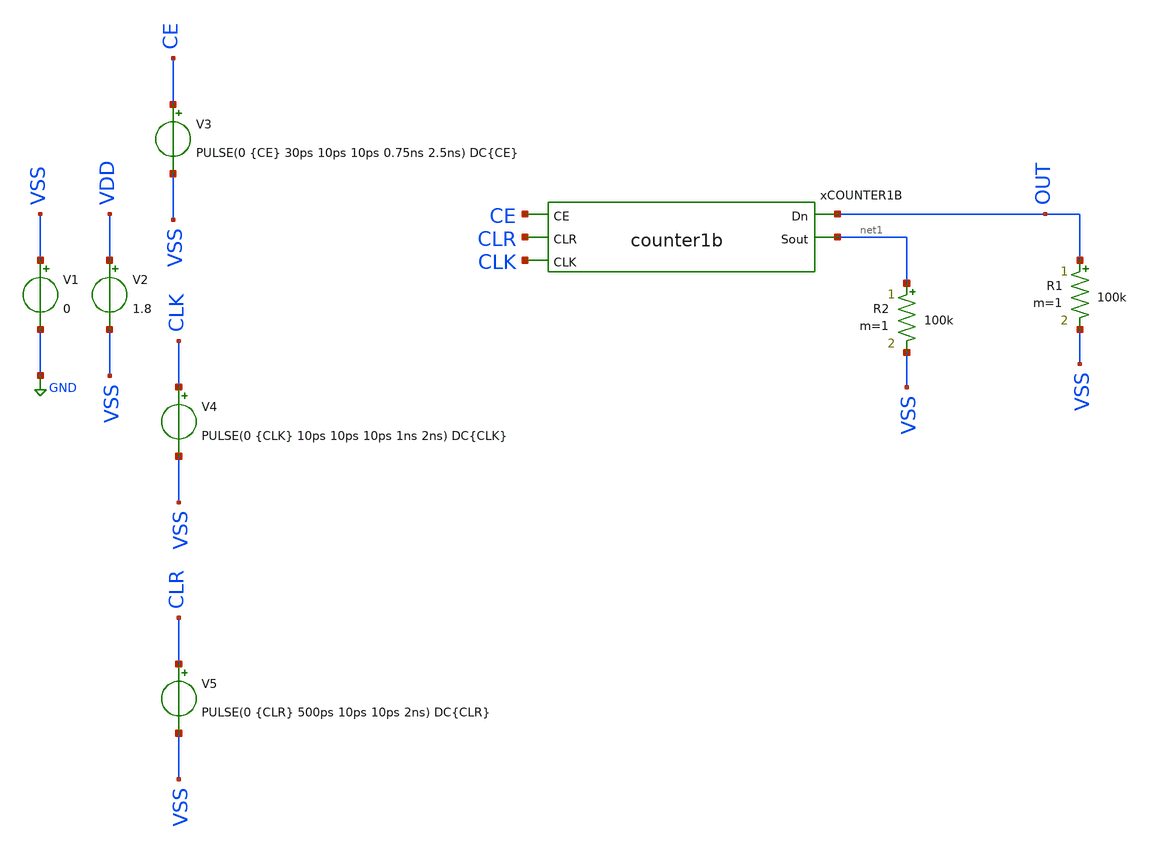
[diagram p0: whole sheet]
** sch_path: track_vlsi/scandaliaris/sch/tb_counter1b.sch
**.subckt tb_counter1b
V1 VSS GND 0
V2 VDD VSS 1.8
V3 CE VSS PULSE(0 {CE} 30ps 10ps 10ps 0.75ns 2.5ns) DC{CE}

V4 CLK VSS PULSE(0 {CLK} 10ps 10ps 10ps 1ns 2ns) DC{CLK}

R1 OUT VSS 100k m=1
V5 CLR VSS PULSE(0 {CLR} 500ps 10ps 10ps 2ns) DC{CLR}
xCOUNTER1B OUT CE CLR CLK net1 VSS VDD counter1b
R2 net1 VSS 100k m=1
**** begin user architecture code


* Parametros del circuito
.param CE = 1.8
.param CLK = 1.8
.param CLR = 1.8
.options TEMP = 27.0

* Include
.lib /home/eamta/skywater/skywater-pdk/libraries/sky130_fd_pr_ngspice/latest/models/corners/sky130.lib TT

* Signals to SAVE
.save all
 + @M.X1.XM1.msky130_fd_pr__nfet_01v8[id]
 + @M.X1.XM1.msky130_fd_pr__nfet_01v8[gm]
 + @M.X1.XM2.msky130_fd_pr__pfet_01v8[id]
 + @M.X1.XM2.msky130_fd_pr__pfet_01v8[gm]

* Simulation
.control
  tran .05n 20ns
  setplot tran1
  plot v(OUT) v(CE) v(CLK) v(CLR)
  *set plot tran2
  *plot @M.X1.XM1.msky130_fd_pr__nfet_01v8[id] @M.X1.XM2.msky130_fd_pr__pfet_01v8[id]
  *set plot tran3
  *plot @M.X1.XM1.msky130_fd_pr__nfet_01v8[gm] @M.X1.XM2.msky130_fd_pr__pfet_01v8[gm]
  *set filetype=ascii
  write tb_dffc_tran.raw

  reset
  *dc V3 0 1.8 0.01
  *setplot dc1
  *plot v(OUT) v(VINA) v(VINB)
  *write tb_dffc_dc.raw

  *reset
  *op
  *save all
  *write tb_dffc.raw
  *print all
.endc

.end


**** end user architecture code
**.ends
.GLOBAL GND
.end
